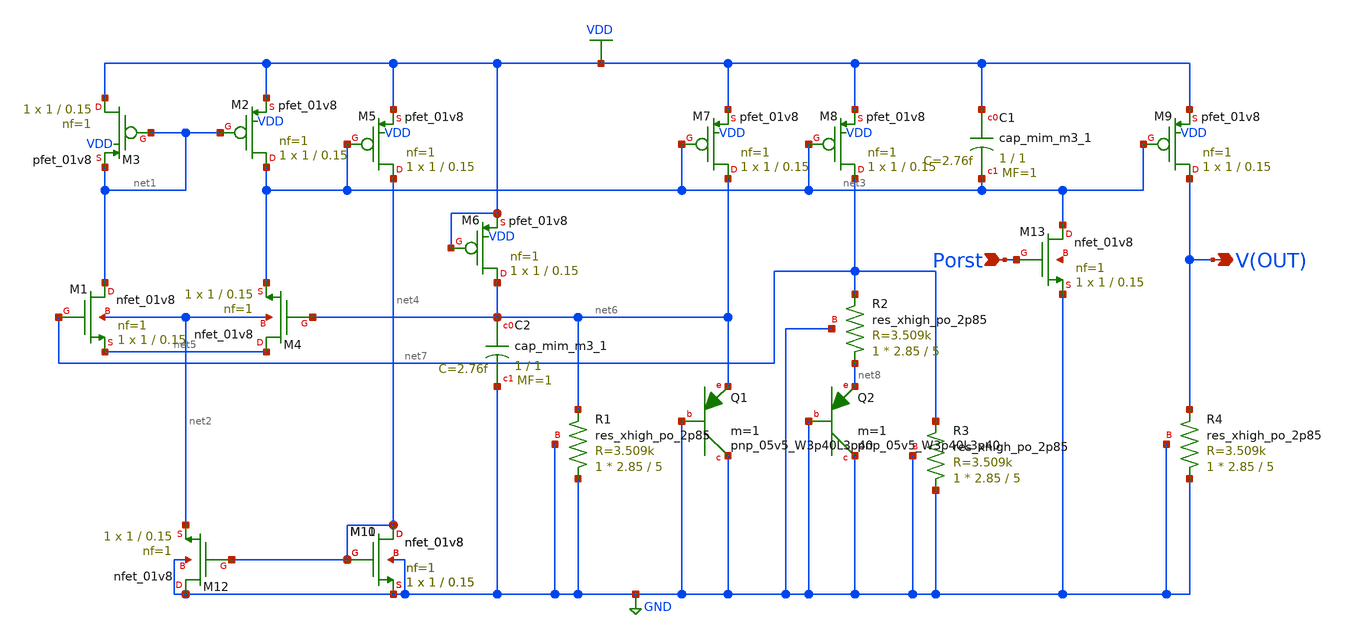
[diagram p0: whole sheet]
** sch_path: bgr.sch
**.subckt bgr Porst V(OUT)
*.ipin Porst
*.opin V(OUT)
XM1 net1 net7 net5 net2 sky130_fd_pr__nfet_01v8 L=0.15 W=1 nf=1 ad='int((nf+1)/2) * W/nf * 0.29' as='int((nf+2)/2) * W/nf * 0.29'
+ pd='2*int((nf+1)/2) * (W/nf + 0.29)' ps='2*int((nf+2)/2) * (W/nf + 0.29)' nrd='0.29 / W' nrs='0.29 / W'
+ sa=0 sb=0 sd=0 mult=1 m=1
XM2 net3 net1 VDD VDD sky130_fd_pr__pfet_01v8 L=0.15 W=1 nf=1 ad='int((nf+1)/2) * W/nf * 0.29' as='int((nf+2)/2) * W/nf * 0.29'
+ pd='2*int((nf+1)/2) * (W/nf + 0.29)' ps='2*int((nf+2)/2) * (W/nf + 0.29)' nrd='0.29 / W' nrs='0.29 / W'
+ sa=0 sb=0 sd=0 mult=1 m=1
XM3 VDD net1 net1 VDD sky130_fd_pr__pfet_01v8 L=0.15 W=1 nf=1 ad='int((nf+1)/2) * W/nf * 0.29' as='int((nf+2)/2) * W/nf * 0.29'
+ pd='2*int((nf+1)/2) * (W/nf + 0.29)' ps='2*int((nf+2)/2) * (W/nf + 0.29)' nrd='0.29 / W' nrs='0.29 / W'
+ sa=0 sb=0 sd=0 mult=1 m=1
XM4 net5 net6 net3 net2 sky130_fd_pr__nfet_01v8 L=0.15 W=1 nf=1 ad='int((nf+1)/2) * W/nf * 0.29' as='int((nf+2)/2) * W/nf * 0.29'
+ pd='2*int((nf+1)/2) * (W/nf + 0.29)' ps='2*int((nf+2)/2) * (W/nf + 0.29)' nrd='0.29 / W' nrs='0.29 / W'
+ sa=0 sb=0 sd=0 mult=1 m=1
XM5 net4 net3 VDD VDD sky130_fd_pr__pfet_01v8 L=0.15 W=1 nf=1 ad='int((nf+1)/2) * W/nf * 0.29' as='int((nf+2)/2) * W/nf * 0.29'
+ pd='2*int((nf+1)/2) * (W/nf + 0.29)' ps='2*int((nf+2)/2) * (W/nf + 0.29)' nrd='0.29 / W' nrs='0.29 / W'
+ sa=0 sb=0 sd=0 mult=1 m=1
XM6 net6 VDD VDD VDD sky130_fd_pr__pfet_01v8 L=0.15 W=1 nf=1 ad='int((nf+1)/2) * W/nf * 0.29' as='int((nf+2)/2) * W/nf * 0.29'
+ pd='2*int((nf+1)/2) * (W/nf + 0.29)' ps='2*int((nf+2)/2) * (W/nf + 0.29)' nrd='0.29 / W' nrs='0.29 / W'
+ sa=0 sb=0 sd=0 mult=1 m=1
XM7 net6 net3 VDD VDD sky130_fd_pr__pfet_01v8 L=0.15 W=1 nf=1 ad='int((nf+1)/2) * W/nf * 0.29' as='int((nf+2)/2) * W/nf * 0.29'
+ pd='2*int((nf+1)/2) * (W/nf + 0.29)' ps='2*int((nf+2)/2) * (W/nf + 0.29)' nrd='0.29 / W' nrs='0.29 / W'
+ sa=0 sb=0 sd=0 mult=1 m=1
XM8 net7 net3 VDD VDD sky130_fd_pr__pfet_01v8 L=0.15 W=1 nf=1 ad='int((nf+1)/2) * W/nf * 0.29' as='int((nf+2)/2) * W/nf * 0.29'
+ pd='2*int((nf+1)/2) * (W/nf + 0.29)' ps='2*int((nf+2)/2) * (W/nf + 0.29)' nrd='0.29 / W' nrs='0.29 / W'
+ sa=0 sb=0 sd=0 mult=1 m=1
XM9 V(OUT) net3 VDD VDD sky130_fd_pr__pfet_01v8 L=0.15 W=1 nf=1 ad='int((nf+1)/2) * W/nf * 0.29' as='int((nf+2)/2) * W/nf * 0.29'
+ pd='2*int((nf+1)/2) * (W/nf + 0.29)' ps='2*int((nf+2)/2) * (W/nf + 0.29)' nrd='0.29 / W' nrs='0.29 / W'
+ sa=0 sb=0 sd=0 mult=1 m=1
XC1 VDD net3 sky130_fd_pr__cap_mim_m3_1 W=1 L=1 MF=1 m=1
XM11 net4 net4 GND GND sky130_fd_pr__nfet_01v8 L=0.15 W=1 nf=1 ad='int((nf+1)/2) * W/nf * 0.29' as='int((nf+2)/2) * W/nf * 0.29'
+ pd='2*int((nf+1)/2) * (W/nf + 0.29)' ps='2*int((nf+2)/2) * (W/nf + 0.29)' nrd='0.29 / W' nrs='0.29 / W'
+ sa=0 sb=0 sd=0 mult=1 m=1
XM12 GND net4 net2 GND sky130_fd_pr__nfet_01v8 L=0.15 W=1 nf=1 ad='int((nf+1)/2) * W/nf * 0.29' as='int((nf+2)/2) * W/nf * 0.29'
+ pd='2*int((nf+1)/2) * (W/nf + 0.29)' ps='2*int((nf+2)/2) * (W/nf + 0.29)' nrd='0.29 / W' nrs='0.29 / W'
+ sa=0 sb=0 sd=0 mult=1 m=1
XC2 net6 GND sky130_fd_pr__cap_mim_m3_1 W=1 L=1 MF=1 m=1
XR1 GND net6 GND sky130_fd_pr__res_xhigh_po_2p85 L=5 mult=1 m=1
XQ1 GND GND net6 sky130_fd_pr__pnp_05v5_W3p40L3p40 m=1
XQ2 GND GND net8 sky130_fd_pr__pnp_05v5_W3p40L3p40 m=1
XR2 net8 net7 GND sky130_fd_pr__res_xhigh_po_2p85 L=5 mult=1 m=1
XR3 GND net7 GND sky130_fd_pr__res_xhigh_po_2p85 L=5 mult=1 m=1
XR4 GND V(OUT) GND sky130_fd_pr__res_xhigh_po_2p85 L=5 mult=1 m=1
XM10 net4 net4 GND GND sky130_fd_pr__nfet_01v8 L=0.15 W=1 nf=1 ad='int((nf+1)/2) * W/nf * 0.29' as='int((nf+2)/2) * W/nf * 0.29'
+ pd='2*int((nf+1)/2) * (W/nf + 0.29)' ps='2*int((nf+2)/2) * (W/nf + 0.29)' nrd='0.29 / W' nrs='0.29 / W'
+ sa=0 sb=0 sd=0 mult=1 m=1
XM13 net3 Porst GND net9 sky130_fd_pr__nfet_01v8 L=0.15 W=1 nf=1 ad='int((nf+1)/2) * W/nf * 0.29' as='int((nf+2)/2) * W/nf * 0.29'
+ pd='2*int((nf+1)/2) * (W/nf + 0.29)' ps='2*int((nf+2)/2) * (W/nf + 0.29)' nrd='0.29 / W' nrs='0.29 / W'
+ sa=0 sb=0 sd=0 mult=1 m=1
**.ends
.GLOBAL VDD
.GLOBAL GND
.end
